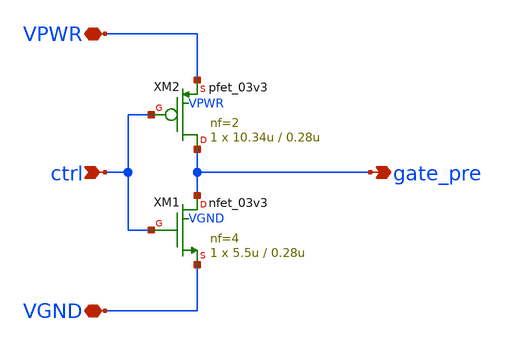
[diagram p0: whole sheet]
** sch_path: pg/gf180mcuD/common/xschem/gate_predrv_3v3.sch
**.subckt gate_predrv_3v3 VPWR VGND ctrl gate_pre
*.iopin VPWR
*.iopin VGND
*.ipin ctrl
*.opin gate_pre
XM1 gate_pre ctrl VGND VGND nfet_03v3 L=0.28u W=5.5u nf=4 ad='int((nf+1)/2) * W/nf * 0.18u' as='int((nf+2)/2) * W/nf * 0.18u'
+ pd='2*int((nf+1)/2) * (W/nf + 0.18u)' ps='2*int((nf+2)/2) * (W/nf + 0.18u)' nrd='0.18u / W' nrs='0.18u / W'
+ sa=0 sb=0 sd=0 m=1 par=1
XM2 gate_pre ctrl VPWR VPWR pfet_03v3 L=0.28u W=10.34u nf=2 ad='int((nf+1)/2) * W/nf * 0.18u' as='int((nf+2)/2) * W/nf * 0.18u'
+ pd='2*int((nf+1)/2) * (W/nf + 0.18u)' ps='2*int((nf+2)/2) * (W/nf + 0.18u)' nrd='0.18u / W' nrs='0.18u / W'
+ sa=0 sb=0 sd=0 m=1 par=1
**.ends
.end
